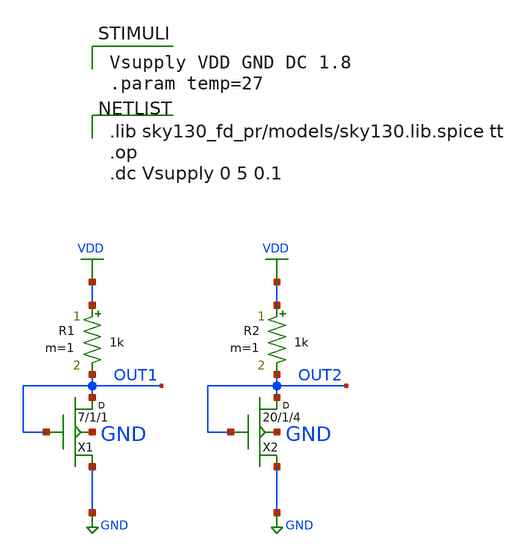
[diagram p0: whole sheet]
** sch_path: tool-test/tooltest.sch
**.subckt tooltest
X1 OUT1 OUT1 GND GND sky130_fd_pr__nfet_01v8 w=7 l=1 m=1
R1 VDD OUT1 1k m=1
X2 OUT2 OUT2 GND GND sky130_fd_pr__nfet_g5v0d10v5 w=20 l=1 m=4
R2 VDD OUT2 1k m=1
**** begin user architecture code

.lib sky130_fd_pr/models/sky130.lib.spice tt
.op
.dc Vsupply 0 5 0.1


Vsupply VDD GND DC 1.8
.param temp=27

**** end user architecture code
**.ends
.GLOBAL GND
.GLOBAL VDD
.end
